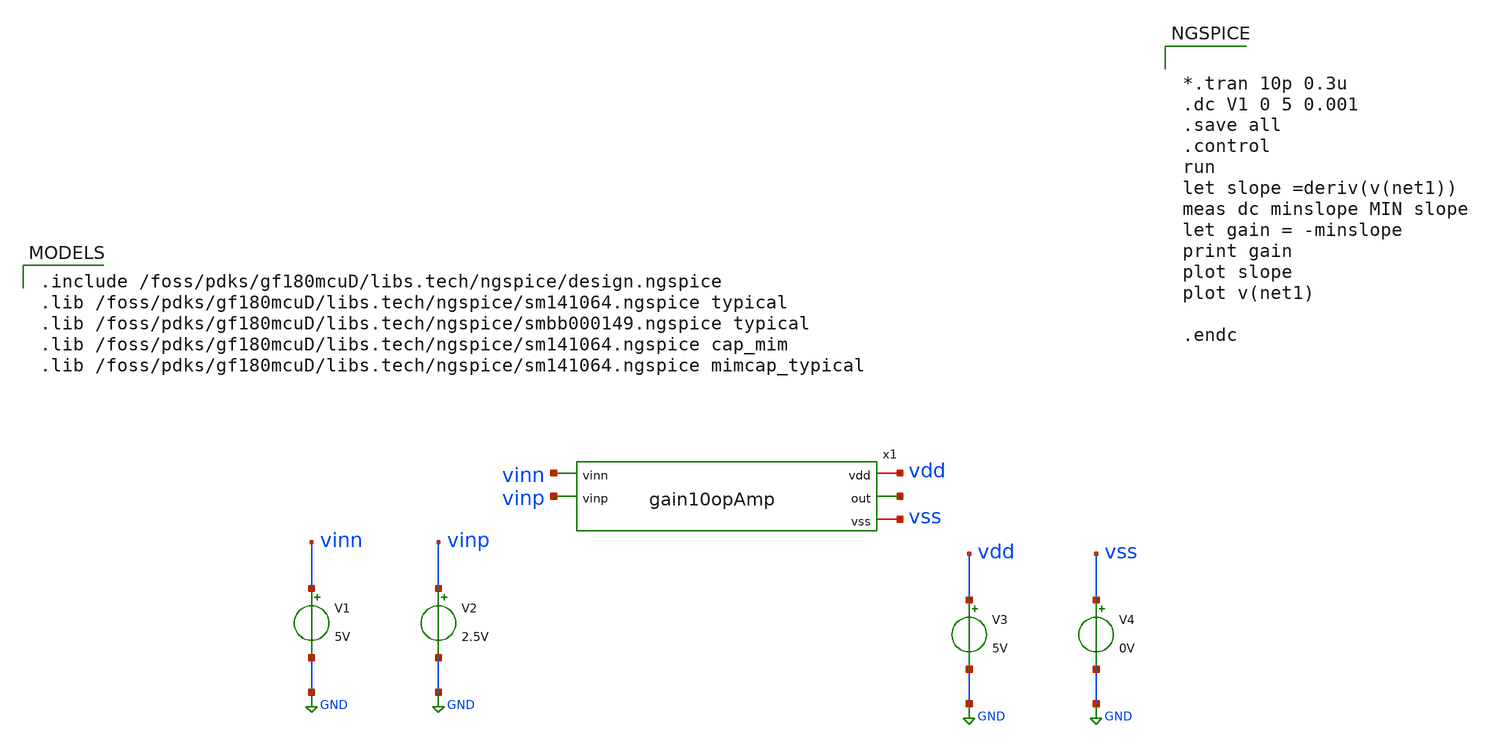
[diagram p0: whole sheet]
** sch_path: activities/opamp2AKAM/simulations_testbench/simulations_testbench/gain10OpAmpSweep.sch
**.subckt gain10OpAmpSweep
V1 vinn GND 5V
V2 vinp GND 2.5V
V3 vdd GND 5V
V4 vss GND 0V
x1 vdd vinn net1 vinp vss gain10opAmp
**** begin user architecture code

.include /foss/pdks/gf180mcuD/libs.tech/ngspice/design.ngspice
.lib /foss/pdks/gf180mcuD/libs.tech/ngspice/sm141064.ngspice typical
.lib /foss/pdks/gf180mcuD/libs.tech/ngspice/smbb000149.ngspice typical
.lib /foss/pdks/gf180mcuD/libs.tech/ngspice/sm141064.ngspice cap_mim
.lib /foss/pdks/gf180mcuD/libs.tech/ngspice/sm141064.ngspice mimcap_typical



*.tran 10p 0.3u
.dc V1 0 5 0.001
.save all
.control
run
let slope =deriv(v(net1))
meas dc minslope MIN slope
let gain = -minslope
print gain
plot slope
plot v(net1)

.endc

**** end user architecture code
**.ends
.GLOBAL GND
.end
